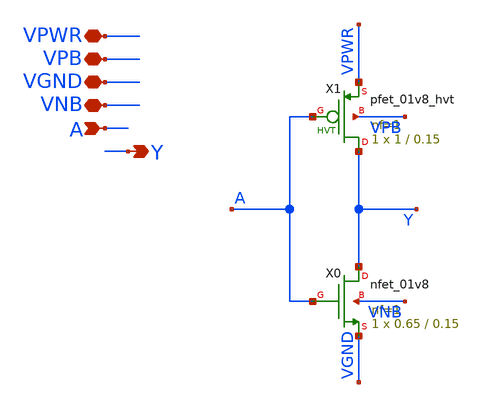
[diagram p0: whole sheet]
** sch_path: analog/klayout/production/final_merge_20260923/testbenches/cace/analog/xschem/sky130_fd_sc_hd__inv_1.sch
**.subckt sky130_fd_sc_hd__inv_1 A Y VNB VPB VPWR VGND
*.ipin A
*.opin Y
*.iopin VNB
*.iopin VPB
*.iopin VPWR
*.iopin VGND
XX0 Y A VGND VNB sky130_fd_pr__nfet_01v8 L=0.15 W=0.65 nf=1 ad='int((1 + 1)/2) * 0.65 / 1 * 0.29' as='int((1 + 2)/2) * 0.65 / 1 * 0.29'
+ pd='2*int((1 + 1)/2) * (0.65 / 1 + 0.29)' ps='2*int((1 + 2)/2) * (0.65 / 1 + 0.29)' nrd='0.29 / 0.65 '
+ nrs='0.29 / 0.65 ' sa=0 sb=0 sd=0 mult=1 m=1
XX1 Y A VPWR VPB sky130_fd_pr__pfet_01v8_hvt L=0.15 W=1 nf=1 ad='int((1 + 1)/2) * 1 / 1 * 0.29' as='int((1 + 2)/2) * 1 / 1 * 0.29'
+ pd='2*int((1 + 1)/2) * (1 / 1 + 0.29)' ps='2*int((1 + 2)/2) * (1 / 1 + 0.29)' nrd='0.29 / 1 ' nrs='0.29 / 1 '
+ sa=0 sb=0 sd=0 mult=1 m=1
**.ends
.end
